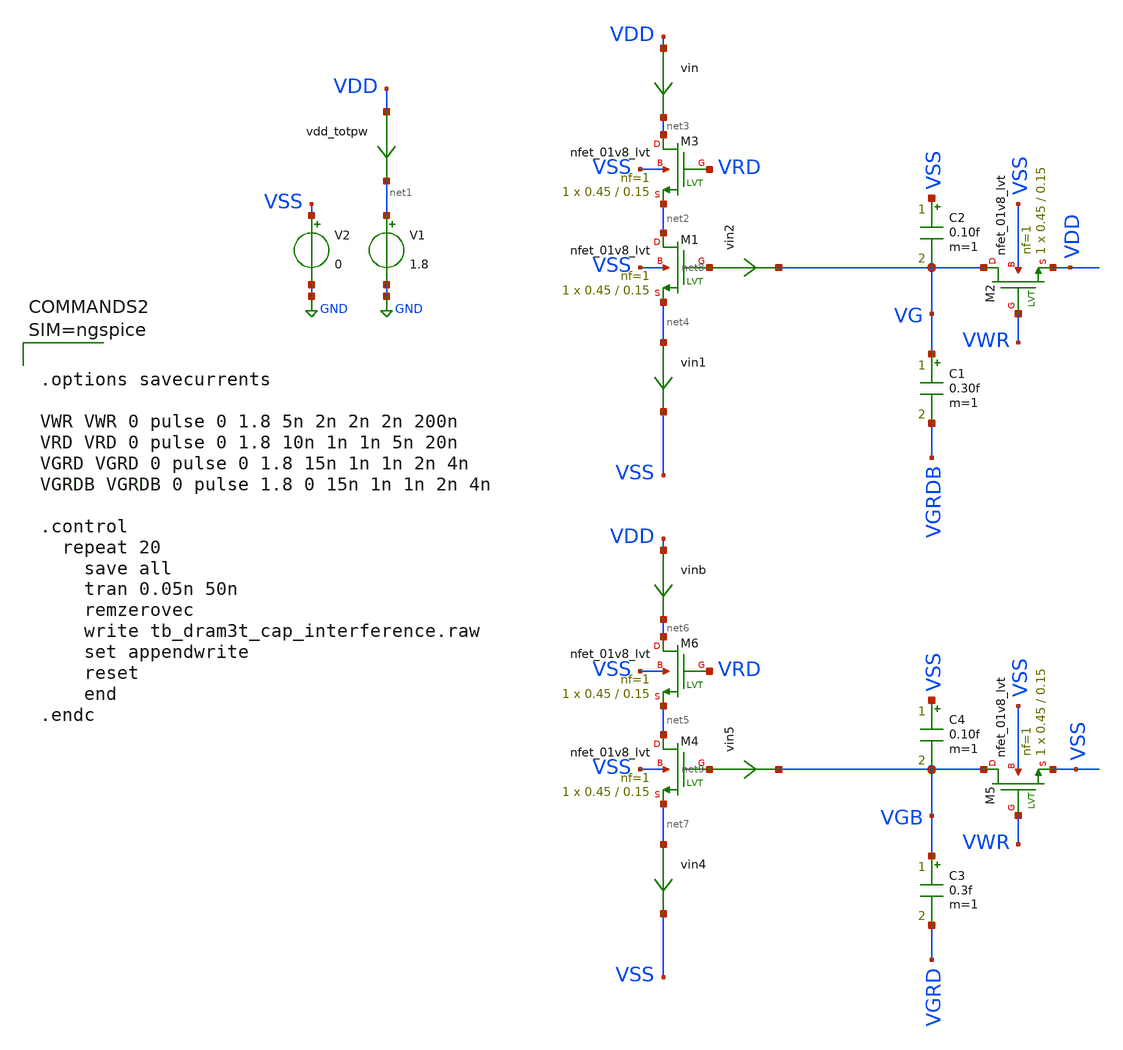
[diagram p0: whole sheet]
** sch_path: xschem/tb_dram3t_cap_interference.sch
**.subckt tb_dram3t_cap_interference
V1 net1 GND 1.8
V2 VSS GND 0
vdd_totpw VDD net1 0
.save i(vdd_totpw)
vin VDD net3 0
.save i(vin)
XM1 net2 net8 net4 VSS sky130_fd_pr__nfet_01v8_lvt L=0.15 W=0.45 nf=1 ad='int((nf+1)/2) * W/nf * 0.29'
+ as='int((nf+2)/2) * W/nf * 0.29' pd='2*int((nf+1)/2) * (W/nf + 0.29)' ps='2*int((nf+2)/2) * (W/nf + 0.29)'
+ nrd='0.29 / W' nrs='0.29 / W' sa=0 sb=0 sd=0 mult=1 m=1
XM2 VG VWR VDD VSS sky130_fd_pr__nfet_01v8_lvt L=0.15 W=0.45 nf=1 ad='int((nf+1)/2) * W/nf * 0.29' as='int((nf+2)/2) * W/nf * 0.29'
+ pd='2*int((nf+1)/2) * (W/nf + 0.29)' ps='2*int((nf+2)/2) * (W/nf + 0.29)' nrd='0.29 / W' nrs='0.29 / W'
+ sa=0 sb=0 sd=0 mult=1 m=1
XM3 net3 VRD net2 VSS sky130_fd_pr__nfet_01v8_lvt L=0.15 W=0.45 nf=1 ad='int((nf+1)/2) * W/nf * 0.29'
+ as='int((nf+2)/2) * W/nf * 0.29' pd='2*int((nf+1)/2) * (W/nf + 0.29)' ps='2*int((nf+2)/2) * (W/nf + 0.29)'
+ nrd='0.29 / W' nrs='0.29 / W' sa=0 sb=0 sd=0 mult=1 m=1
C1 VG VGRDB 0.30f m=1
C2 VSS VG 0.10f m=1
vin1 net4 VSS 0
.save i(vin1)
vin2 net8 VG 0
.save i(vin2)
vinb VDD net6 0
.save i(vinb)
XM4 net5 net9 net7 VSS sky130_fd_pr__nfet_01v8_lvt L=0.15 W=0.45 nf=1 ad='int((nf+1)/2) * W/nf * 0.29'
+ as='int((nf+2)/2) * W/nf * 0.29' pd='2*int((nf+1)/2) * (W/nf + 0.29)' ps='2*int((nf+2)/2) * (W/nf + 0.29)'
+ nrd='0.29 / W' nrs='0.29 / W' sa=0 sb=0 sd=0 mult=1 m=1
XM5 VGB VWR VSS VSS sky130_fd_pr__nfet_01v8_lvt L=0.15 W=0.45 nf=1 ad='int((nf+1)/2) * W/nf * 0.29' as='int((nf+2)/2) * W/nf * 0.29'
+ pd='2*int((nf+1)/2) * (W/nf + 0.29)' ps='2*int((nf+2)/2) * (W/nf + 0.29)' nrd='0.29 / W' nrs='0.29 / W'
+ sa=0 sb=0 sd=0 mult=1 m=1
XM6 net6 VRD net5 VSS sky130_fd_pr__nfet_01v8_lvt L=0.15 W=0.45 nf=1 ad='int((nf+1)/2) * W/nf * 0.29'
+ as='int((nf+2)/2) * W/nf * 0.29' pd='2*int((nf+1)/2) * (W/nf + 0.29)' ps='2*int((nf+2)/2) * (W/nf + 0.29)'
+ nrd='0.29 / W' nrs='0.29 / W' sa=0 sb=0 sd=0 mult=1 m=1
C3 VGB VGRD 0.3f m=1
C4 VSS VGB 0.10f m=1
vin4 net7 VSS 0
.save i(vin4)
vin5 net9 VGB 0
.save i(vin5)
**** begin user architecture code

** opencircuitdesign pdks install
.lib $::SKYWATER_MODELS/sky130.lib.spice tt_mm
*.lib $::SKYWATER_STDCELLS/sky130_fd_sc_hd_blablabla.spice

.subckt sky130_fd_sc_hd__inv_1 A VGND VNB VPB VPWR Y
X0 VGND A Y VNB sky130_fd_pr__nfet_01v8 w=650000u l=150000u
X1 VPWR A Y VPB sky130_fd_pr__pfet_01v8_hvt w=1e+06u l=150000u
.ends





.options savecurrents

VWR VWR 0 pulse 0 1.8 5n 2n 2n 2n 200n
VRD VRD 0 pulse 0 1.8 10n 1n 1n 5n 20n
VGRD VGRD 0 pulse 0 1.8 15n 1n 1n 2n 4n
VGRDB VGRDB 0 pulse 1.8 0 15n 1n 1n 2n 4n

.control
  repeat 20
    save all
    tran 0.05n 50n
    remzerovec
    write tb_dram3t_cap_interference.raw
    set appendwrite
    reset
    end
.endc






**** end user architecture code
**.ends
.GLOBAL GND
.end
